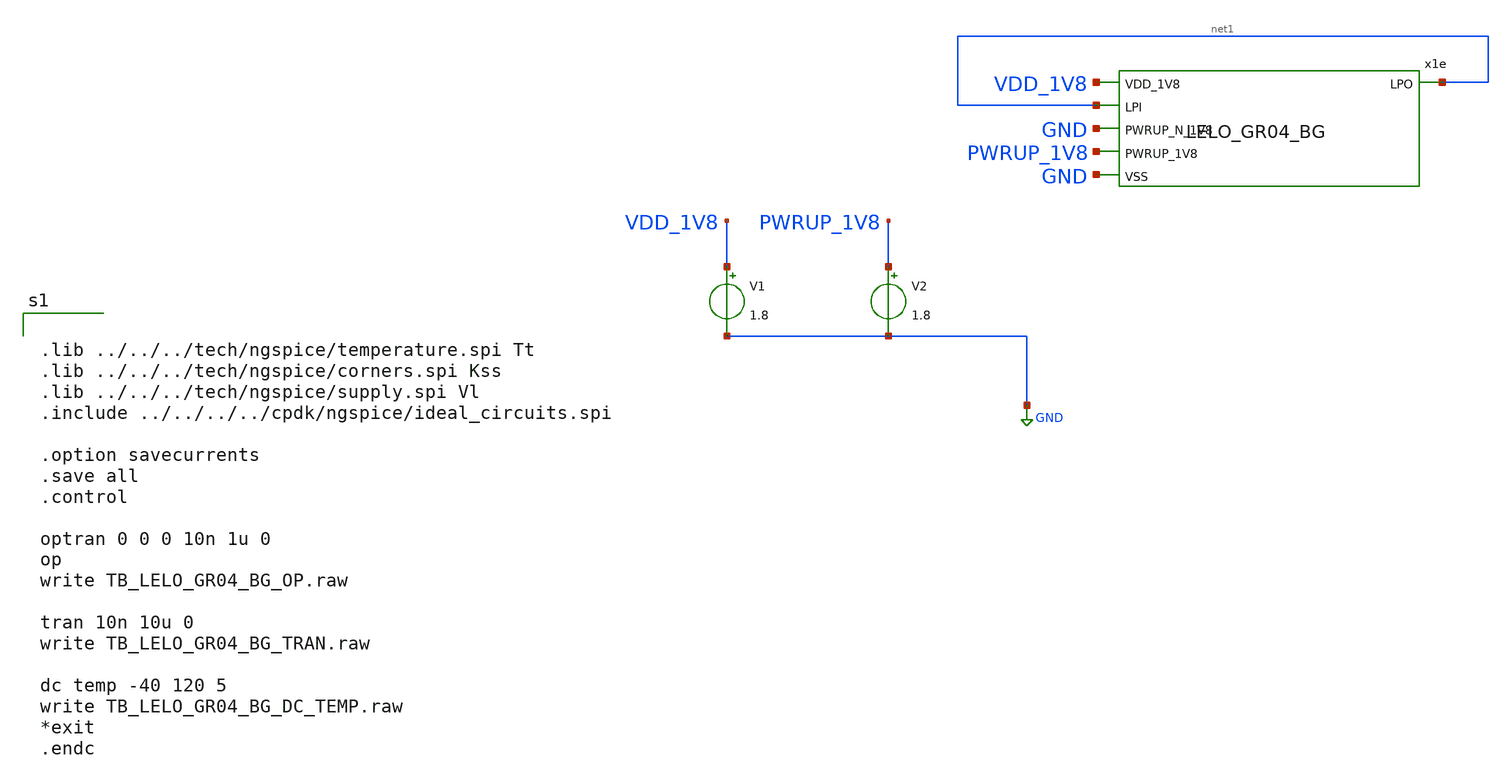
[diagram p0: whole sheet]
** sch_path: design/LELO_GR04_SKY130A/TB_LELO_GR04_BG.sch
**.subckt TB_LELO_GR04_BG
x1e VDD_1V8 net1 net1 GND PWRUP_1V8 GND LELO_GR04_BG
V1 VDD_1V8 GND 1.8
V2 PWRUP_1V8 GND 1.8
**** begin user architecture code


.lib ../../../tech/ngspice/temperature.spi Tt
.lib ../../../tech/ngspice/corners.spi Kss
.lib ../../../tech/ngspice/supply.spi Vl
.include ../../../../cpdk/ngspice/ideal_circuits.spi

.option savecurrents
.save all
.control

optran 0 0 0 10n 1u 0
op
write TB_LELO_GR04_BG_OP.raw

tran 10n 10u 0
write TB_LELO_GR04_BG_TRAN.raw

dc temp -40 120 5
write TB_LELO_GR04_BG_DC_TEMP.raw
*exit
.endc


**** end user architecture code
**.ends
.GLOBAL GND
.end
